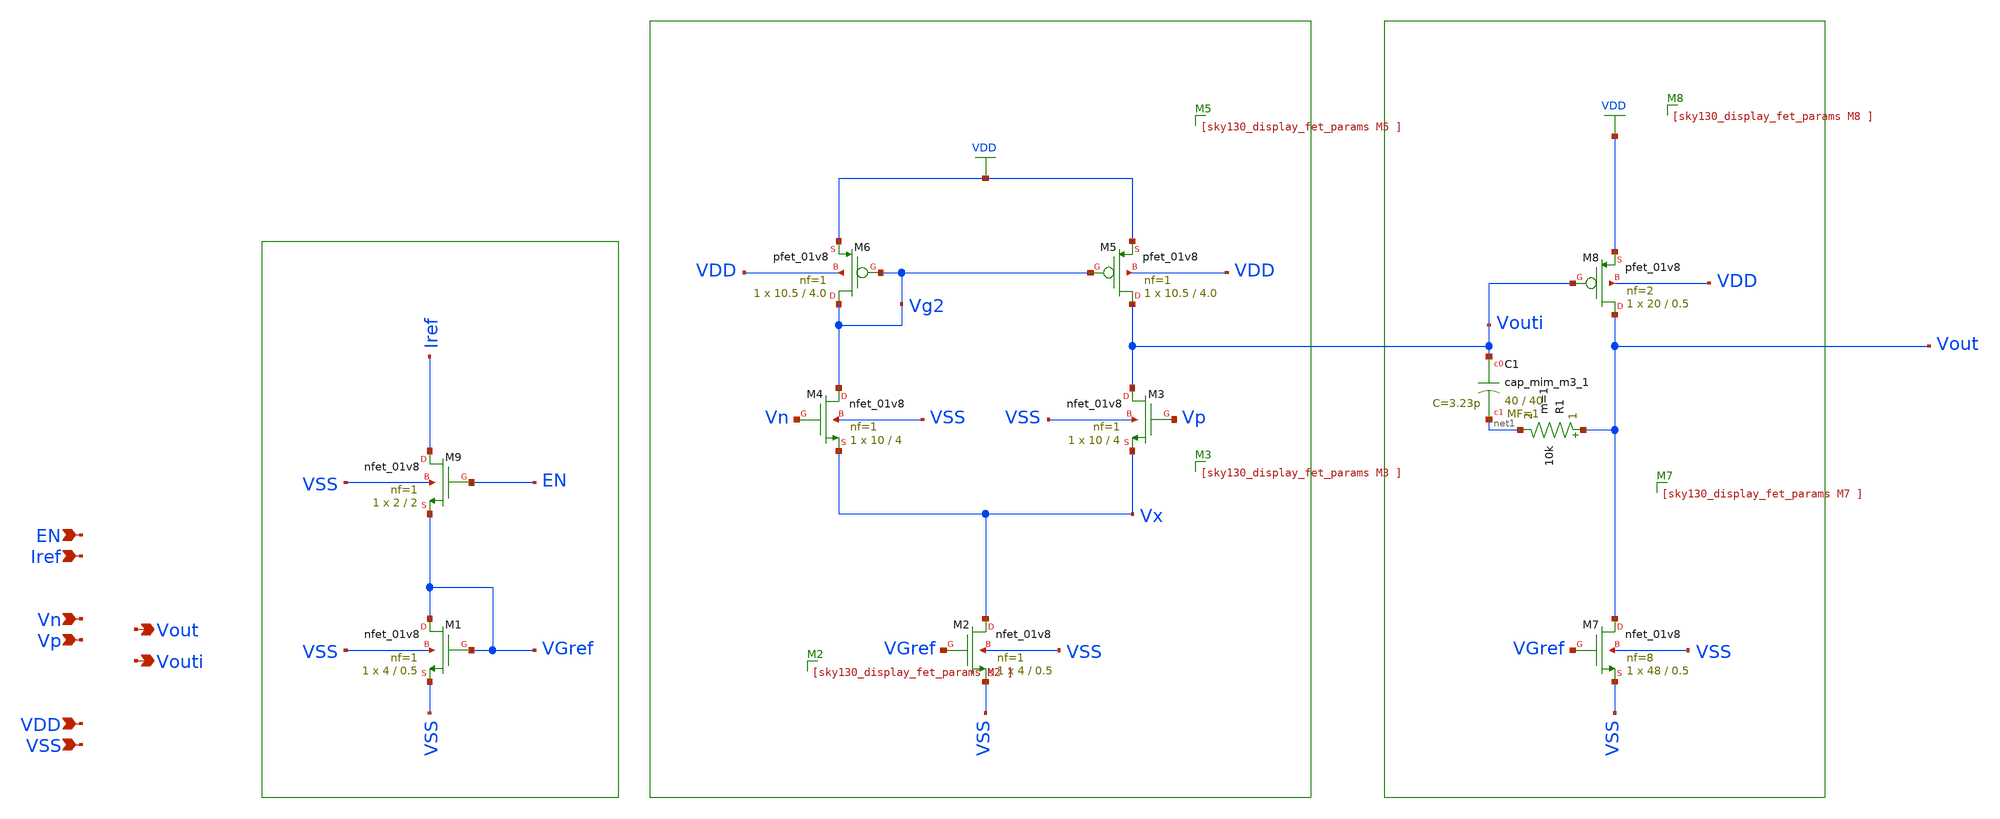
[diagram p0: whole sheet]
** sch_path: xschem/opamp.sch
**.subckt opamp VSS Vp Vout Vn VDD Iref Vouti EN
*.ipin VSS
*.ipin Vp
*.opin Vout
*.ipin Vn
*.ipin VDD
*.ipin Iref
*.opin Vouti
*.ipin EN
XM1 VGref VGref VSS VSS sky130_fd_pr__nfet_01v8 L=0.5 W=4 nf=1 ad='int((1 + 1)/2) * 4 / 1 * 0.29' as='int((1 + 2)/2) * 4 / 1 * 0.29'
+ pd='2*int((1 + 1)/2) * (4 / 1 + 0.29)' ps='2*int((1 + 2)/2) * (4 / 1 + 0.29)' nrd='0.29 / 4 ' nrs='0.29 / 4 '
+ sa=0 sb=0 sd=0 mult=1 m=1
XM2 Vx VGref VSS VSS sky130_fd_pr__nfet_01v8 L=0.5 W=4 nf=1 ad='int((1 + 1)/2) * 4 / 1 * 0.29' as='int((1 + 2)/2) * 4 / 1 * 0.29'
+ pd='2*int((1 + 1)/2) * (4 / 1 + 0.29)' ps='2*int((1 + 2)/2) * (4 / 1 + 0.29)' nrd='0.29 / 4 ' nrs='0.29 / 4 '
+ sa=0 sb=0 sd=0 mult=1 m=1
XM3 Vouti Vp Vx VSS sky130_fd_pr__nfet_01v8 L=4 W=10 nf=1 ad='int((1 + 1)/2) * 10 / 1 * 0.29' as='int((1 + 2)/2) * 10 / 1 * 0.29'
+ pd='2*int((1 + 1)/2) * (10 / 1 + 0.29)' ps='2*int((1 + 2)/2) * (10 / 1 + 0.29)' nrd='0.29 / 10 ' nrs='0.29 / 10 '
+ sa=0 sb=0 sd=0 mult=1 m=1
XM4 Vg2 Vn Vx VSS sky130_fd_pr__nfet_01v8 L=4 W=10 nf=1 ad='int((1 + 1)/2) * 10 / 1 * 0.29' as='int((1 + 2)/2) * 10 / 1 * 0.29'
+ pd='2*int((1 + 1)/2) * (10 / 1 + 0.29)' ps='2*int((1 + 2)/2) * (10 / 1 + 0.29)' nrd='0.29 / 10 ' nrs='0.29 / 10 '
+ sa=0 sb=0 sd=0 mult=1 m=1
XM5 Vouti Vg2 VDD VDD sky130_fd_pr__pfet_01v8 L=4.0 W=10.5 nf=1 ad='int((1 + 1)/2) * 10.5 / 1 * 0.29'
+ as='int((1 + 2)/2) * 10.5 / 1 * 0.29' pd='2*int((1 + 1)/2) * (10.5 / 1 + 0.29)' ps='2*int((1 + 2)/2) * (10.5 / 1 + 0.29)'
+ nrd='0.29 / 10.5 ' nrs='0.29 / 10.5 ' sa=0 sb=0 sd=0 mult=1 m=1
XM6 Vg2 Vg2 VDD VDD sky130_fd_pr__pfet_01v8 L=4.0 W=10.5 nf=1 ad='int((1 + 1)/2) * 10.5 / 1 * 0.29' as='int((1 + 2)/2) * 10.5 / 1 * 0.29'
+ pd='2*int((1 + 1)/2) * (10.5 / 1 + 0.29)' ps='2*int((1 + 2)/2) * (10.5 / 1 + 0.29)' nrd='0.29 / 10.5 '
+ nrs='0.29 / 10.5 ' sa=0 sb=0 sd=0 mult=1 m=1
XM7 Vout VGref VSS VSS sky130_fd_pr__nfet_01v8 L=0.5 W=48 nf=8 ad='int((8 + 1)/2) * 48 / 8 * 0.29' as='int((8 + 2)/2) * 48 / 8 * 0.29'
+ pd='2*int((8 + 1)/2) * (48 / 8 + 0.29)' ps='2*int((8 + 2)/2) * (48 / 8 + 0.29)' nrd='0.29 / 48 ' nrs='0.29 / 48 '
+ sa=0 sb=0 sd=0 mult=1 m=1
XM8 Vout Vouti VDD VDD sky130_fd_pr__pfet_01v8 L=0.5 W=20 nf=2 ad='int((2 + 1)/2) * 20 / 2 * 0.29' as='int((2 + 2)/2) * 20 / 2 * 0.29'
+ pd='2*int((2 + 1)/2) * (20 / 2 + 0.29)' ps='2*int((2 + 2)/2) * (20 / 2 + 0.29)' nrd='0.29 / 20 ' nrs='0.29 / 20 '
+ sa=0 sb=0 sd=0 mult=1 m=1
XM9 Iref EN VGref VSS sky130_fd_pr__nfet_01v8 L=2 W=2 nf=1 ad='int((1 + 1)/2) * 2 / 1 * 0.29' as='int((1 + 2)/2) * 2 / 1 * 0.29'
+ pd='2*int((1 + 1)/2) * (2 / 1 + 0.29)' ps='2*int((1 + 2)/2) * (2 / 1 + 0.29)' nrd='0.29 / 2 ' nrs='0.29 / 2 '
+ sa=0 sb=0 sd=0 mult=1 m=1
R1 Vout net1 10k m=1
XC1 Vouti net1 sky130_fd_pr__cap_mim_m3_1 W=40 L=40 MF=1 m=1
**.ends
.GLOBAL VDD
.end
